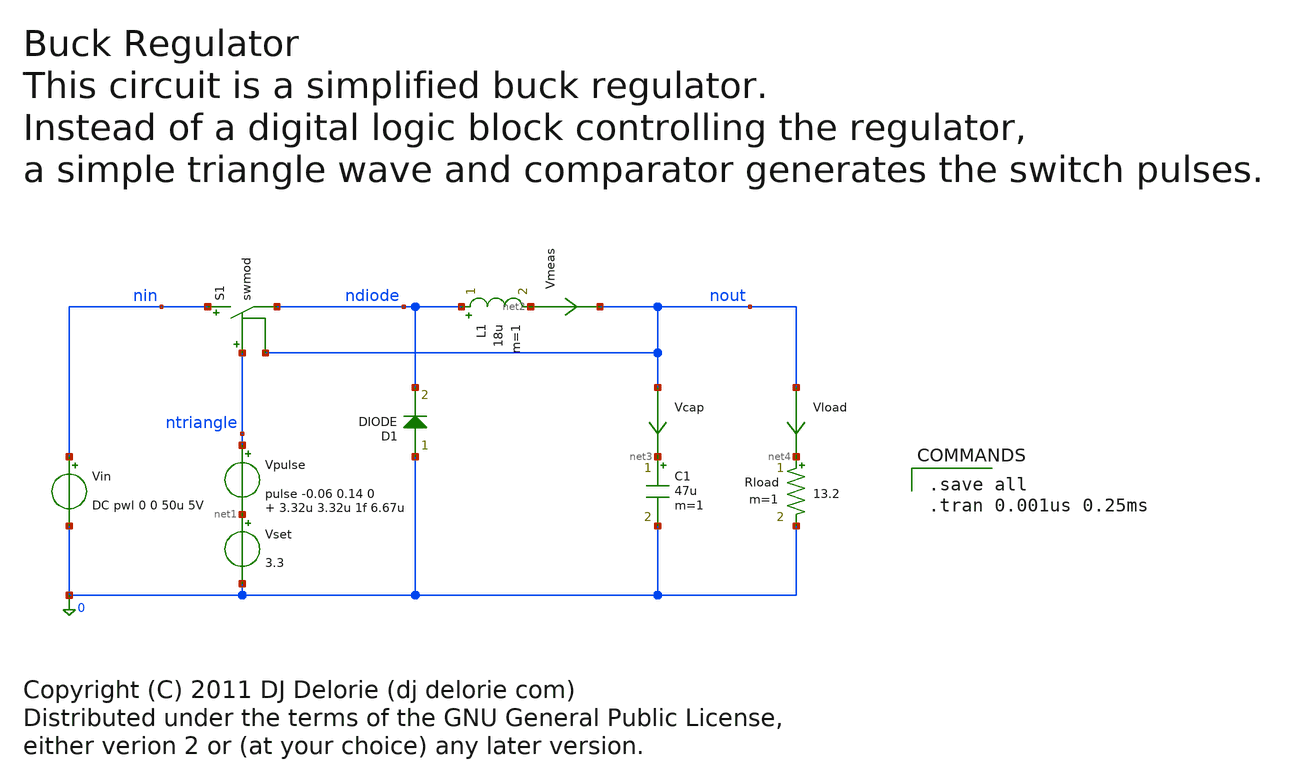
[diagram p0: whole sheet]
** sch_path: xschem_library/ngspice/buck.sch
* Copyright (C) 2011 DJ Delorie (dj delorie com)
* Distributed under the terms of the GNU General Public License,
* either verion 2 or (at your choice) any later version.
**.subckt buck
Vin nin 0 DC pwl 0 0 50u 5V
S1 nin ndiode ntriangle nout swmod
D1 0 ndiode DIODE area=1
Vpulse ntriangle net1 pulse -0.06 0.14 0 3.32u 3.32u 1f 6.67u
Vset net1 0 3.3
Vmeas net2 nout 0
.save i(vmeas)
C1 net3 0 47u m=1
Vcap nout net3 0
.save i(vcap)
Vload nout net4 0
.save i(vload)
Rload net4 0 13.2 m=1
L1 ndiode net2 18u m=1
**** begin user architecture code

.MODEL DIODE D(IS=1.139e-08 RS=0.99 CJO=9.3e-12 VJ=1.6 M=0.411 BV=30 EG=0.7 )
.MODEL swmod SW(VT=0 VH=0.01 RON=1 ROFF=100000)



.save all
.tran 0.001us 0.25ms


**** end user architecture code
**.ends
.end
